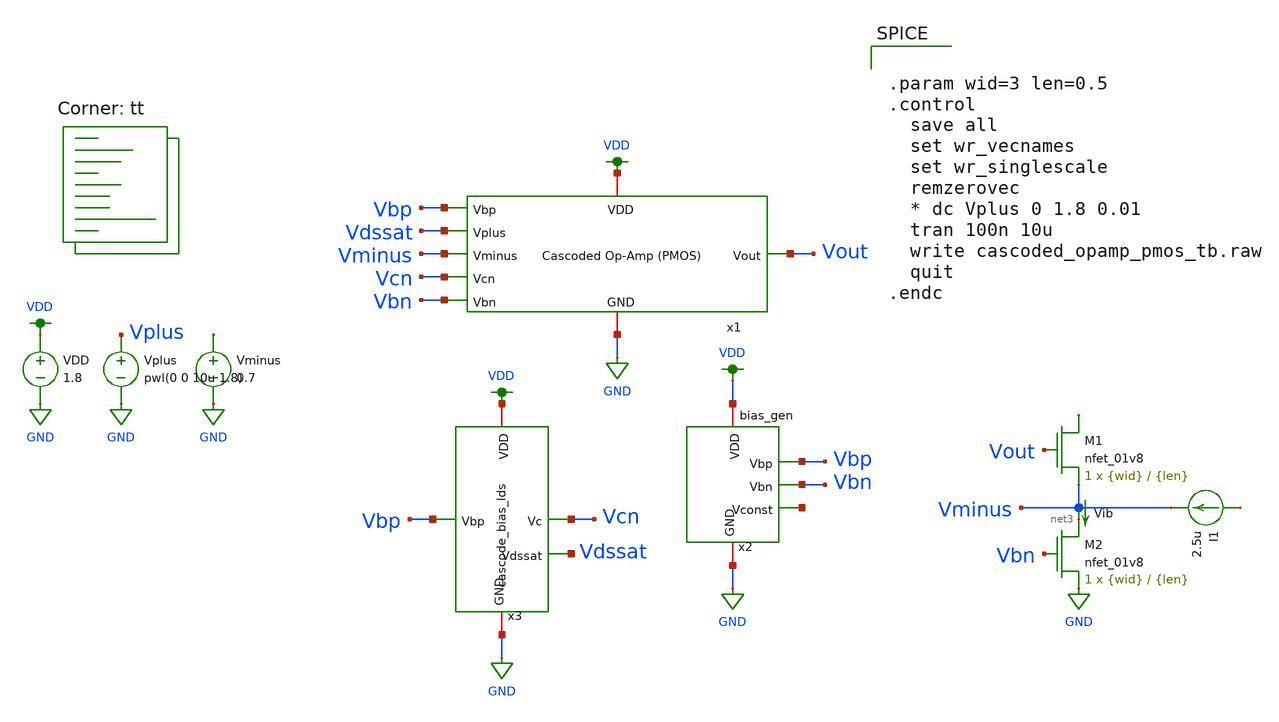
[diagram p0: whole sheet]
** sch_path: final/schematics/cascoded_opamp_pmos_tb.sch
**.subckt cascoded_opamp_pmos_tb
VDD VDD GND 1.8
Vplus Vplus GND pwl(0 0 10u 1.8)
Vminus net1 GND 0.7
x1 Vbp Vdssat Vminus Vcn Vbn VDD GND Vout cascoded_opamp_pmos
x3 Vbp VDD Vcn GND Vdssat cascode_bias_lds
XM1 net2 Vout Vminus GND sky130_fd_pr__nfet_01v8 L={len} W={wid} nf=1 ad='int((nf+1)/2) * W/nf * 0.29'
+ as='int((nf+2)/2) * W/nf * 0.29' pd='2*int((nf+1)/2) * (W/nf + 0.29)' ps='2*int((nf+2)/2) * (W/nf + 0.29)'
+ nrd='0.29 / W' nrs='0.29 / W' sa=0 sb=0 sd=0 mult=1 m=1
XM2 net3 Vbn GND GND sky130_fd_pr__nfet_01v8 L={len} W={wid} nf=1 ad='int((nf+1)/2) * W/nf * 0.29' as='int((nf+2)/2) * W/nf * 0.29'
+ pd='2*int((nf+1)/2) * (W/nf + 0.29)' ps='2*int((nf+2)/2) * (W/nf + 0.29)' nrd='0.29 / W' nrs='0.29 / W'
+ sa=0 sb=0 sd=0 mult=1 m=1
Vib Vminus net3 0
.save i(vib)
I1 net4 Vminus 2.5u
x2 VDD Vbp net5 GND Vbn bias_gen
**** begin user architecture code
.lib $::SKYWATER_MODELS/sky130.lib.spice tt


.param wid=3 len=0.5
.control
  save all
  set wr_vecnames
  set wr_singlescale
  remzerovec
  * dc Vplus 0 1.8 0.01
  tran 100n 10u
  write cascoded_opamp_pmos_tb.raw
  quit
.endc


**** end user architecture code
**.ends
.GLOBAL VDD
.GLOBAL GND
.end
